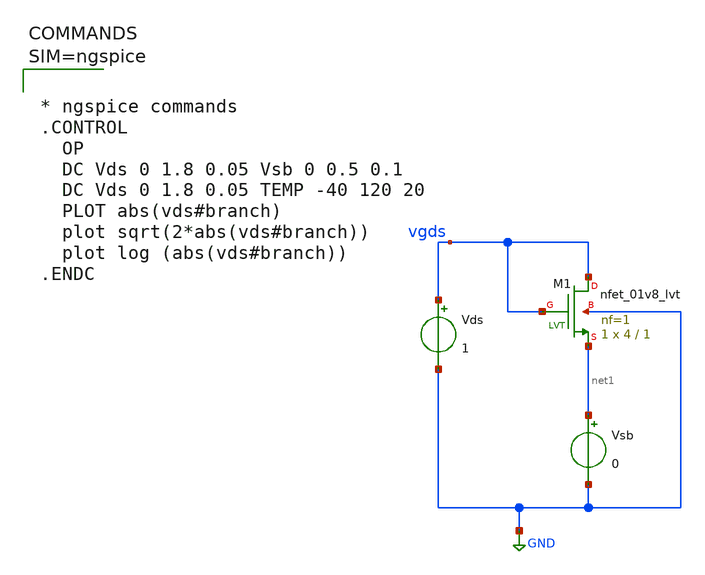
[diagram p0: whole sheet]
** sch_path: xschem/param_extract.sch
**.subckt param_extract
XM1 vgds vgds net1 GND sky130_fd_pr__nfet_01v8_lvt L=1 W=4 nf=1 ad='int((1 + 1)/2) * 4 / 1 * 0.29' as='int((1 + 2)/2) * 4 / 1 * 0.29'
+ pd='2*int((1 + 1)/2) * (4 / 1 + 0.29)' ps='2*int((1 + 2)/2) * (4 / 1 + 0.29)' nrd='0.29 / 4 ' nrs='0.29 / 4 '
+ sa=0 sb=0 sd=0 mult=1 m=1
Vds vgds GND 1
Vsb net1 GND 0
**** begin user architecture code

** opencircuitdesign pdks install
.lib $::SKYWATER_MODELS/sky130.lib.spice tt




* ngspice commands
.CONTROL
  OP
  DC Vds 0 1.8 0.05 Vsb 0 0.5 0.1
  DC Vds 0 1.8 0.05 TEMP -40 120 20
  PLOT abs(vds#branch)
  plot sqrt(2*abs(vds#branch))
  plot log (abs(vds#branch))
.ENDC



**** end user architecture code
**.ends
.GLOBAL GND
.end
